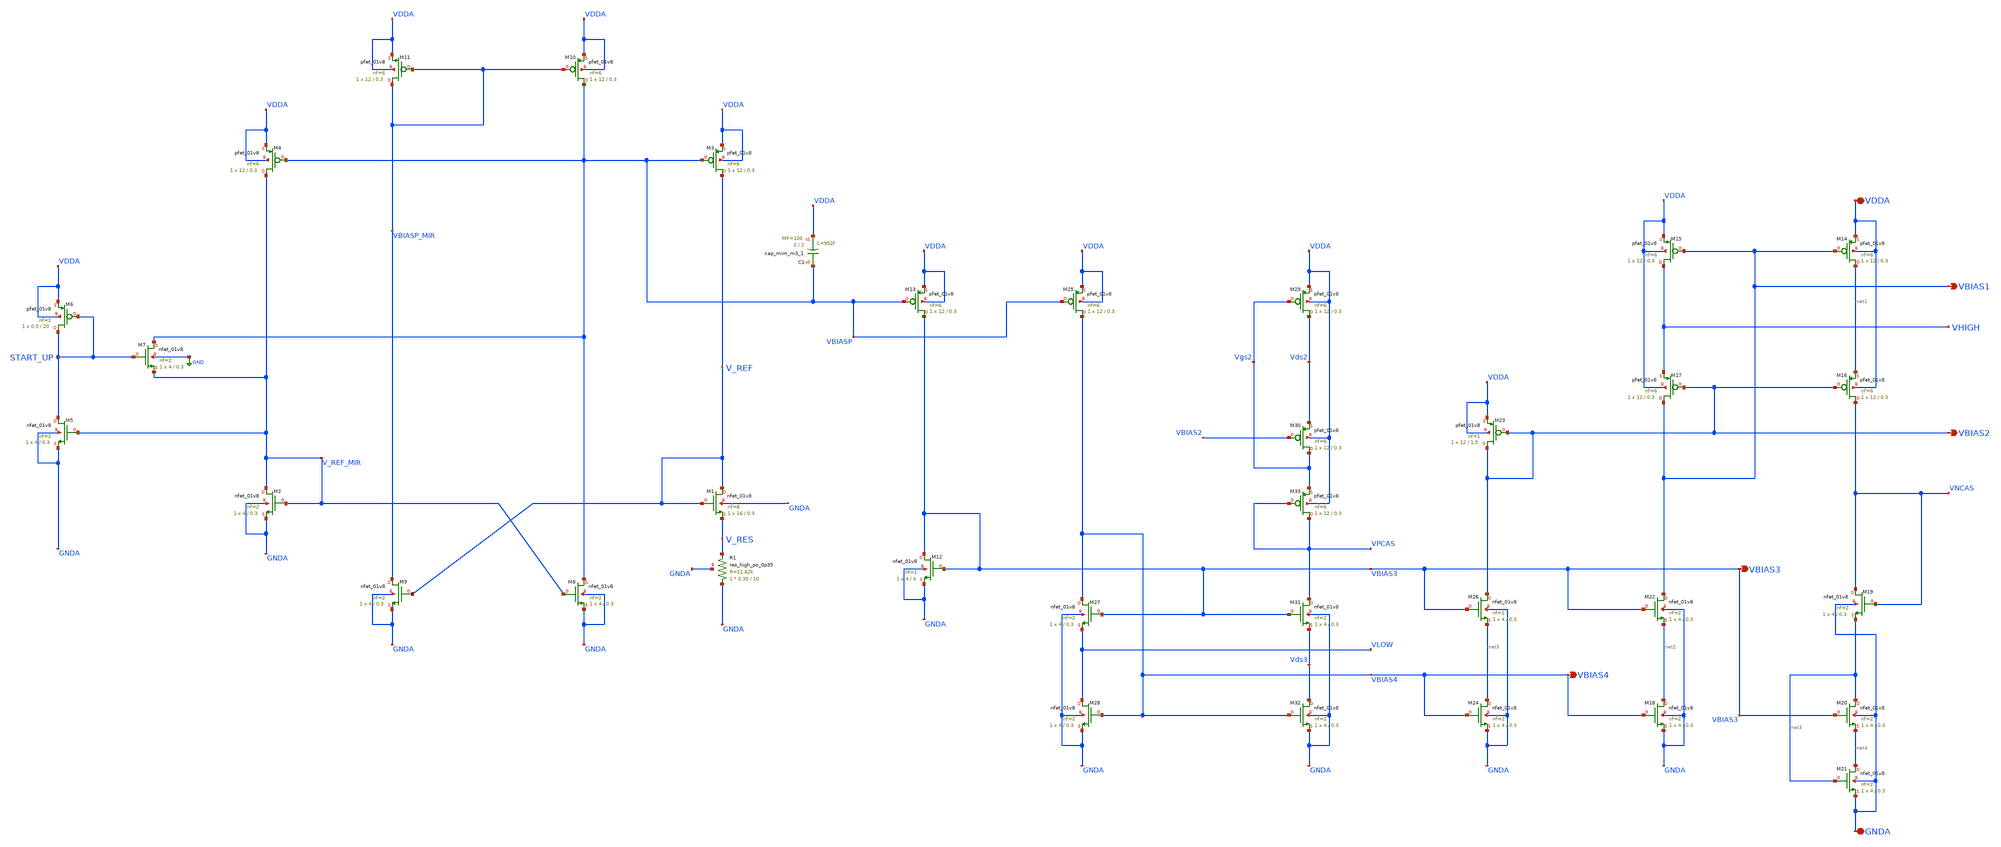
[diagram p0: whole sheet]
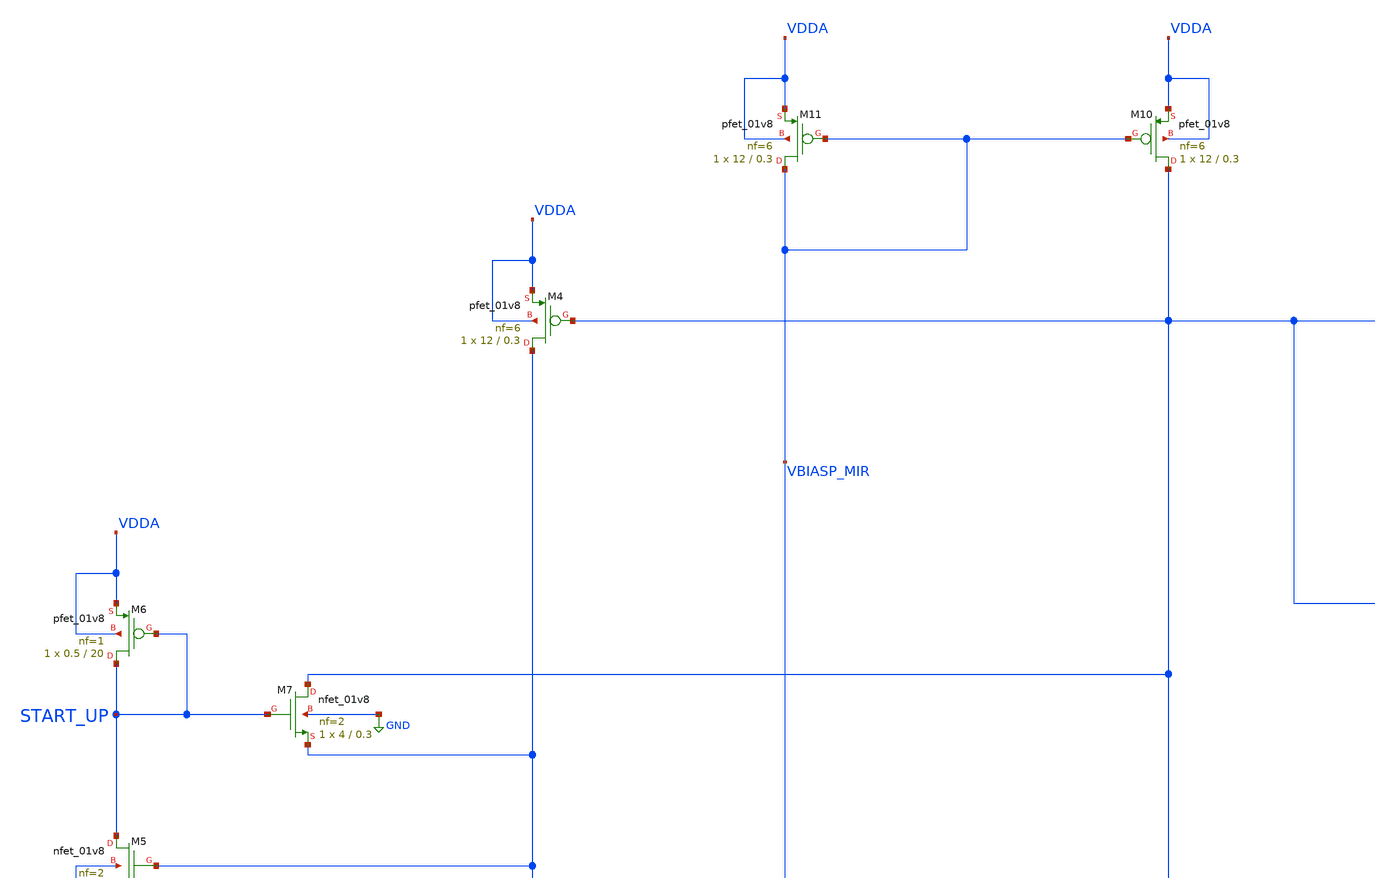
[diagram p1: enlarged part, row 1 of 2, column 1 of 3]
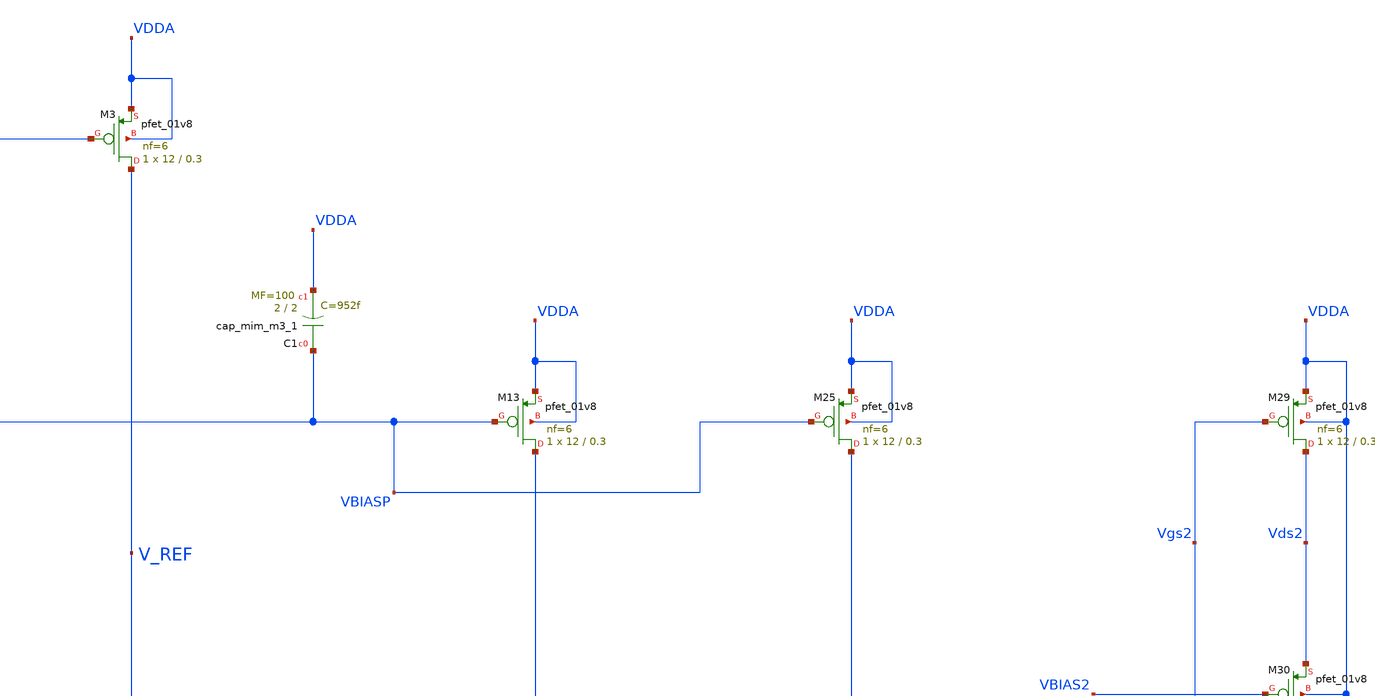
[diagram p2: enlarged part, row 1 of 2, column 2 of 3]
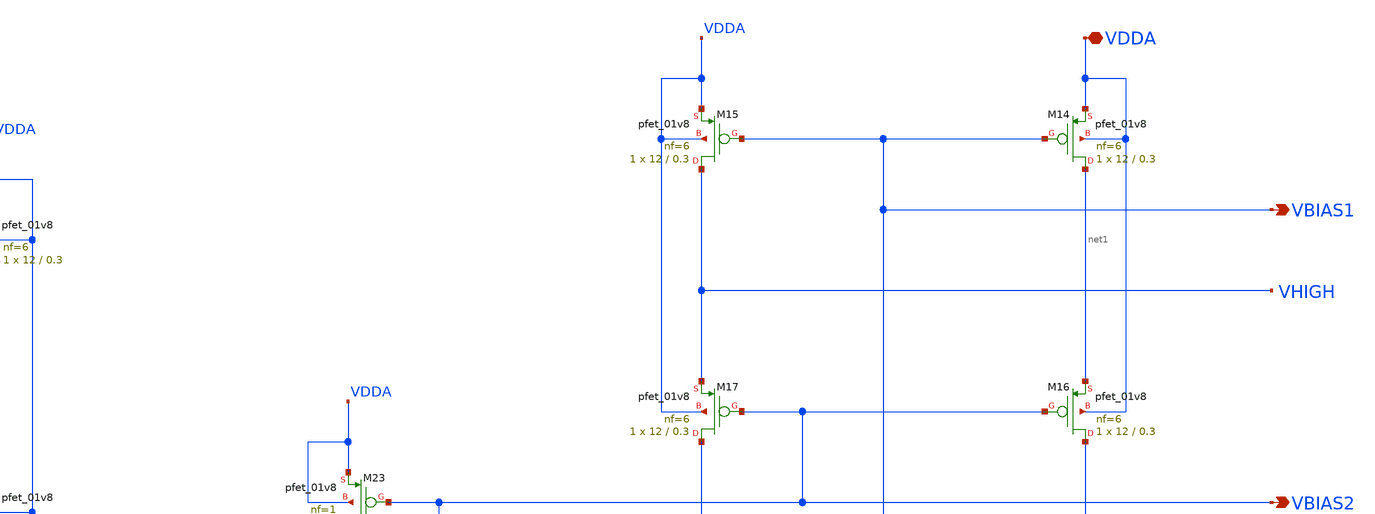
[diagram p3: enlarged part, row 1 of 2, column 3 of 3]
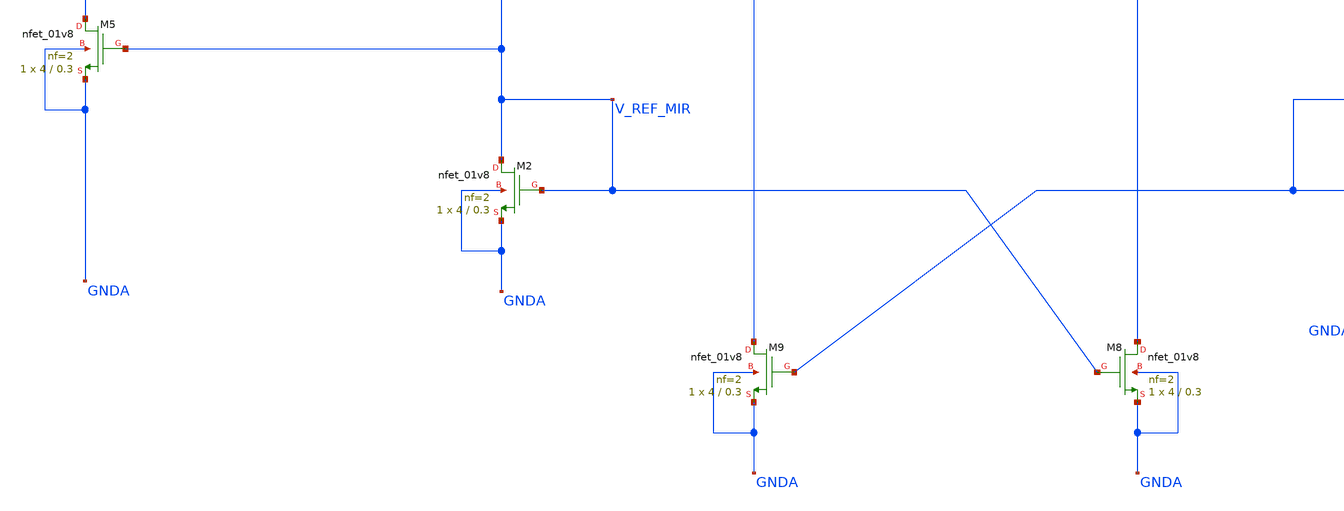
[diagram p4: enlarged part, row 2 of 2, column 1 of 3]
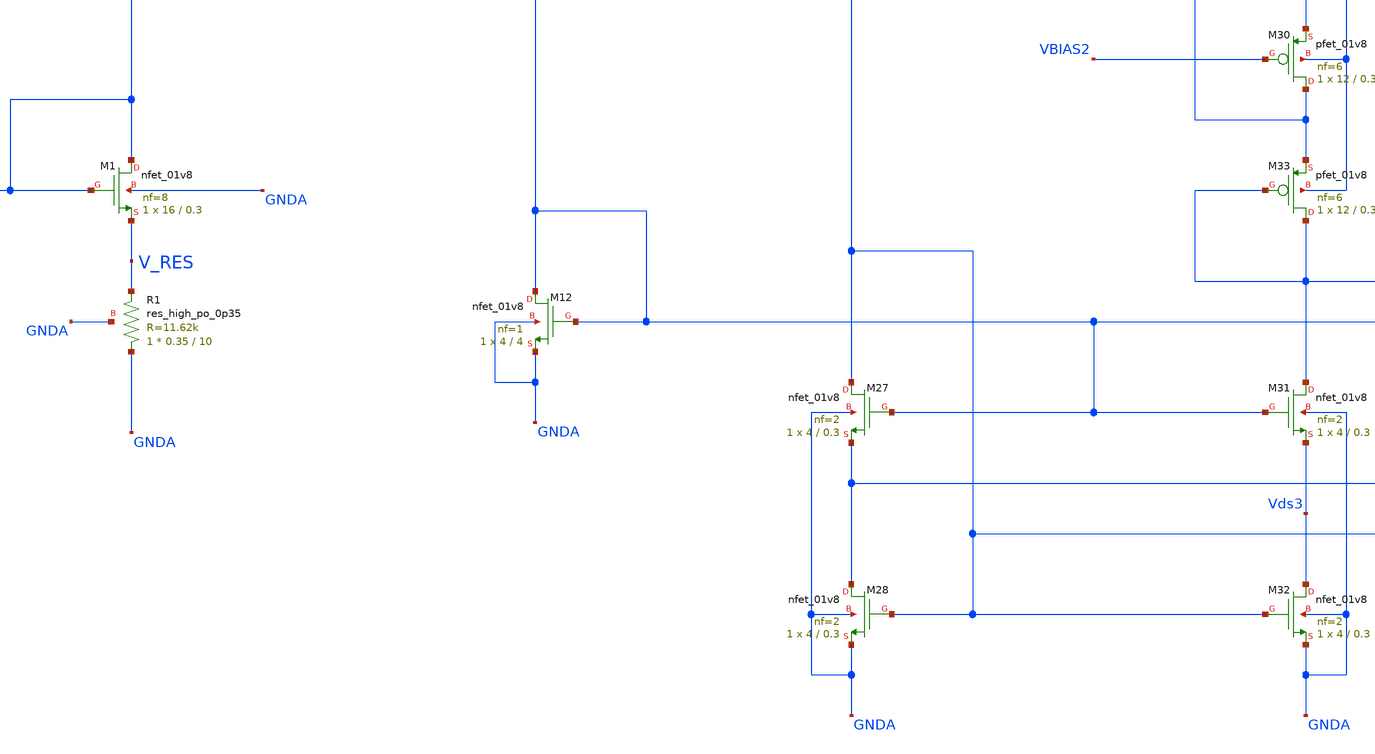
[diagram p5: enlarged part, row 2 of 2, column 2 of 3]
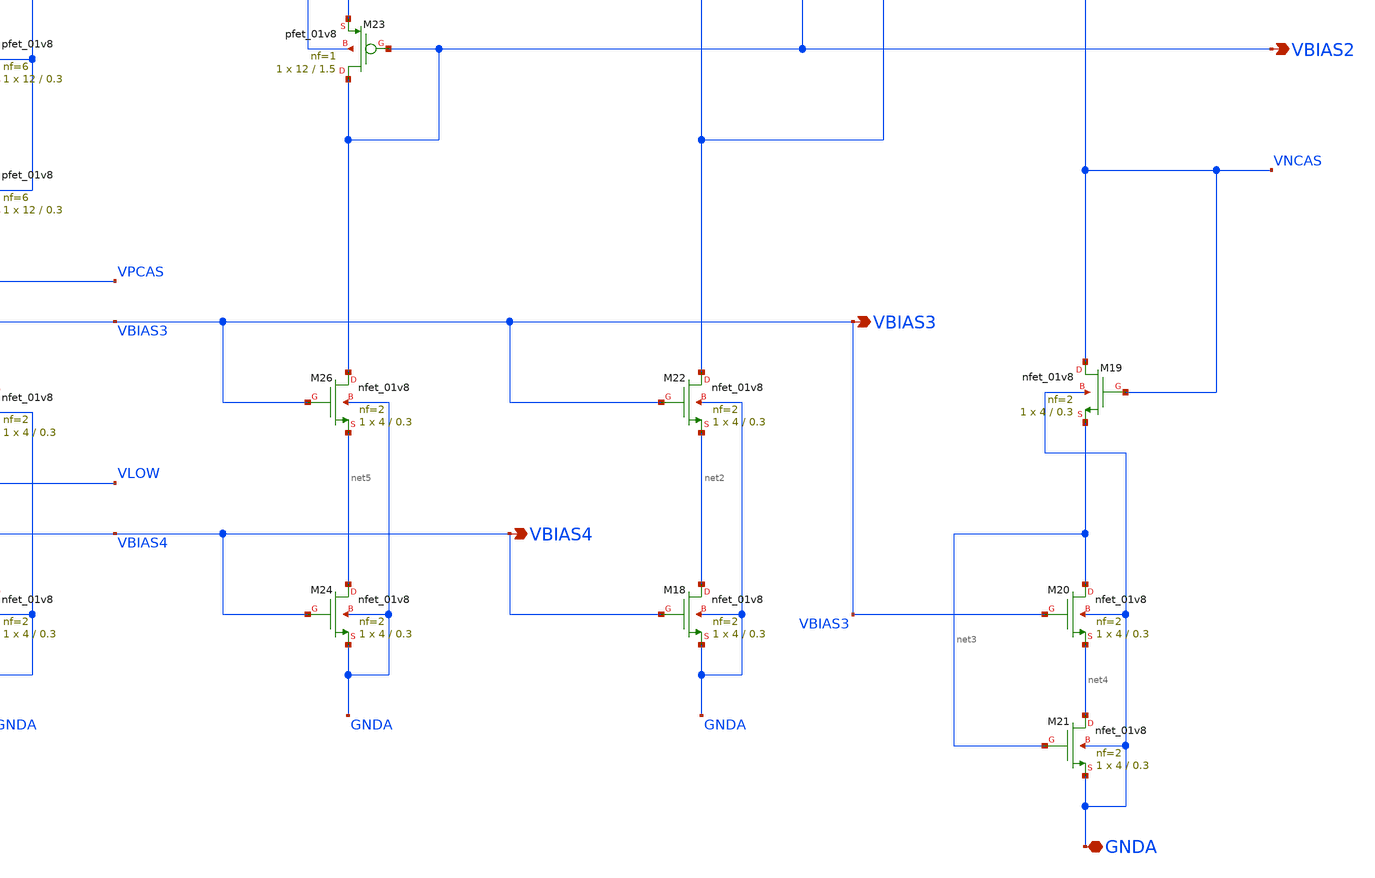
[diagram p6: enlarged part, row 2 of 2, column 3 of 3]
** sch_path: projects/ASU/EEE572/schematic/biasing_circuit.sch
**.subckt biasing_circuit VDDA GNDA VBIAS1 VBIAS2 VBIAS3 VBIAS4
*.iopin VDDA
*.iopin GNDA
*.opin VBIAS1
*.opin VBIAS2
*.opin VBIAS3
*.opin VBIAS4
XM1 V_REF V_REF V_RES GNDA sky130_fd_pr__nfet_01v8 L=0.3 W=16 nf=8 ad='int((nf+1)/2) * W/nf * 0.29' as='int((nf+2)/2) * W/nf * 0.29'
+ pd='2*int((nf+1)/2) * (W/nf + 0.29)' ps='2*int((nf+2)/2) * (W/nf + 0.29)' nrd='0.29 / W' nrs='0.29 / W'
+ sa=0 sb=0 sd=0 mult=1 m=1
XM2 V_REF_MIR V_REF_MIR GNDA GNDA sky130_fd_pr__nfet_01v8 L=0.3 W=4 nf=2 ad='int((nf+1)/2) * W/nf * 0.29'
+ as='int((nf+2)/2) * W/nf * 0.29' pd='2*int((nf+1)/2) * (W/nf + 0.29)' ps='2*int((nf+2)/2) * (W/nf + 0.29)'
+ nrd='0.29 / W' nrs='0.29 / W' sa=0 sb=0 sd=0 mult=1 m=1
XM5 START_UP V_REF_MIR GNDA GNDA sky130_fd_pr__nfet_01v8 L=0.3 W=4 nf=2 ad='int((nf+1)/2) * W/nf * 0.29'
+ as='int((nf+2)/2) * W/nf * 0.29' pd='2*int((nf+1)/2) * (W/nf + 0.29)' ps='2*int((nf+2)/2) * (W/nf + 0.29)'
+ nrd='0.29 / W' nrs='0.29 / W' sa=0 sb=0 sd=0 mult=1 m=1
XM7 VBIASP START_UP V_REF_MIR GND sky130_fd_pr__nfet_01v8 L=0.3 W=4 nf=2 ad='int((nf+1)/2) * W/nf * 0.29'
+ as='int((nf+2)/2) * W/nf * 0.29' pd='2*int((nf+1)/2) * (W/nf + 0.29)' ps='2*int((nf+2)/2) * (W/nf + 0.29)'
+ nrd='0.29 / W' nrs='0.29 / W' sa=0 sb=0 sd=0 mult=1 m=1
XM6 START_UP START_UP VDDA VDDA sky130_fd_pr__pfet_01v8 L=20 W=0.5 nf=1 ad='int((nf+1)/2) * W/nf * 0.29'
+ as='int((nf+2)/2) * W/nf * 0.29' pd='2*int((nf+1)/2) * (W/nf + 0.29)' ps='2*int((nf+2)/2) * (W/nf + 0.29)'
+ nrd='0.29 / W' nrs='0.29 / W' sa=0 sb=0 sd=0 mult=1 m=1
XM3 V_REF VBIASP VDDA VDDA sky130_fd_pr__pfet_01v8 L=0.3 W=12 nf=6 ad='int((nf+1)/2) * W/nf * 0.29' as='int((nf+2)/2) * W/nf * 0.29'
+ pd='2*int((nf+1)/2) * (W/nf + 0.29)' ps='2*int((nf+2)/2) * (W/nf + 0.29)' nrd='0.29 / W' nrs='0.29 / W'
+ sa=0 sb=0 sd=0 mult=1 m=1
XM4 V_REF_MIR VBIASP VDDA VDDA sky130_fd_pr__pfet_01v8 L=0.3 W=12 nf=6 ad='int((nf+1)/2) * W/nf * 0.29'
+ as='int((nf+2)/2) * W/nf * 0.29' pd='2*int((nf+1)/2) * (W/nf + 0.29)' ps='2*int((nf+2)/2) * (W/nf + 0.29)'
+ nrd='0.29 / W' nrs='0.29 / W' sa=0 sb=0 sd=0 mult=1 m=1
XM8 VBIASP V_REF_MIR GNDA GNDA sky130_fd_pr__nfet_01v8 L=0.3 W=4 nf=2 ad='int((nf+1)/2) * W/nf * 0.29'
+ as='int((nf+2)/2) * W/nf * 0.29' pd='2*int((nf+1)/2) * (W/nf + 0.29)' ps='2*int((nf+2)/2) * (W/nf + 0.29)'
+ nrd='0.29 / W' nrs='0.29 / W' sa=0 sb=0 sd=0 mult=1 m=1
XM9 VBIASP_MIR V_REF GNDA GNDA sky130_fd_pr__nfet_01v8 L=0.3 W=4 nf=2 ad='int((nf+1)/2) * W/nf * 0.29'
+ as='int((nf+2)/2) * W/nf * 0.29' pd='2*int((nf+1)/2) * (W/nf + 0.29)' ps='2*int((nf+2)/2) * (W/nf + 0.29)'
+ nrd='0.29 / W' nrs='0.29 / W' sa=0 sb=0 sd=0 mult=1 m=1
XM10 VBIASP VBIASP_MIR VDDA VDDA sky130_fd_pr__pfet_01v8 L=0.3 W=12 nf=6 ad='int((nf+1)/2) * W/nf * 0.29'
+ as='int((nf+2)/2) * W/nf * 0.29' pd='2*int((nf+1)/2) * (W/nf + 0.29)' ps='2*int((nf+2)/2) * (W/nf + 0.29)'
+ nrd='0.29 / W' nrs='0.29 / W' sa=0 sb=0 sd=0 mult=1 m=1
XM11 VBIASP_MIR VBIASP_MIR VDDA VDDA sky130_fd_pr__pfet_01v8 L=0.3 W=12 nf=6 ad='int((nf+1)/2) * W/nf * 0.29'
+ as='int((nf+2)/2) * W/nf * 0.29' pd='2*int((nf+1)/2) * (W/nf + 0.29)' ps='2*int((nf+2)/2) * (W/nf + 0.29)'
+ nrd='0.29 / W' nrs='0.29 / W' sa=0 sb=0 sd=0 mult=1 m=1
XM12 VBIAS3 VBIAS3 GNDA GNDA sky130_fd_pr__nfet_01v8 L=4 W=4 nf=1 ad='int((nf+1)/2) * W/nf * 0.29' as='int((nf+2)/2) * W/nf * 0.29'
+ pd='2*int((nf+1)/2) * (W/nf + 0.29)' ps='2*int((nf+2)/2) * (W/nf + 0.29)' nrd='0.29 / W' nrs='0.29 / W'
+ sa=0 sb=0 sd=0 mult=1 m=1
XM13 VBIAS3 VBIASP VDDA VDDA sky130_fd_pr__pfet_01v8 L=0.3 W=12 nf=6 ad='int((nf+1)/2) * W/nf * 0.29'
+ as='int((nf+2)/2) * W/nf * 0.29' pd='2*int((nf+1)/2) * (W/nf + 0.29)' ps='2*int((nf+2)/2) * (W/nf + 0.29)'
+ nrd='0.29 / W' nrs='0.29 / W' sa=0 sb=0 sd=0 mult=1 m=1
XM14 net1 VBIAS1 VDDA VDDA sky130_fd_pr__pfet_01v8 L=0.3 W=12 nf=6 ad='int((nf+1)/2) * W/nf * 0.29' as='int((nf+2)/2) * W/nf * 0.29'
+ pd='2*int((nf+1)/2) * (W/nf + 0.29)' ps='2*int((nf+2)/2) * (W/nf + 0.29)' nrd='0.29 / W' nrs='0.29 / W'
+ sa=0 sb=0 sd=0 mult=1 m=1
XM15 VHIGH VBIAS1 VDDA VDDA sky130_fd_pr__pfet_01v8 L=0.3 W=12 nf=6 ad='int((nf+1)/2) * W/nf * 0.29'
+ as='int((nf+2)/2) * W/nf * 0.29' pd='2*int((nf+1)/2) * (W/nf + 0.29)' ps='2*int((nf+2)/2) * (W/nf + 0.29)'
+ nrd='0.29 / W' nrs='0.29 / W' sa=0 sb=0 sd=0 mult=1 m=1
XM16 VNCAS VBIAS2 net1 VDDA sky130_fd_pr__pfet_01v8 L=0.3 W=12 nf=6 ad='int((nf+1)/2) * W/nf * 0.29'
+ as='int((nf+2)/2) * W/nf * 0.29' pd='2*int((nf+1)/2) * (W/nf + 0.29)' ps='2*int((nf+2)/2) * (W/nf + 0.29)'
+ nrd='0.29 / W' nrs='0.29 / W' sa=0 sb=0 sd=0 mult=1 m=1
XM17 VBIAS1 VBIAS2 VHIGH VDDA sky130_fd_pr__pfet_01v8 L=0.3 W=12 nf=6 ad='int((nf+1)/2) * W/nf * 0.29'
+ as='int((nf+2)/2) * W/nf * 0.29' pd='2*int((nf+1)/2) * (W/nf + 0.29)' ps='2*int((nf+2)/2) * (W/nf + 0.29)'
+ nrd='0.29 / W' nrs='0.29 / W' sa=0 sb=0 sd=0 mult=1 m=1
XM18 net2 VBIAS4 GNDA GNDA sky130_fd_pr__nfet_01v8 L=0.3 W=4 nf=2 ad='int((nf+1)/2) * W/nf * 0.29' as='int((nf+2)/2) * W/nf * 0.29'
+ pd='2*int((nf+1)/2) * (W/nf + 0.29)' ps='2*int((nf+2)/2) * (W/nf + 0.29)' nrd='0.29 / W' nrs='0.29 / W'
+ sa=0 sb=0 sd=0 mult=1 m=1
XM19 VNCAS VNCAS net3 GNDA sky130_fd_pr__nfet_01v8 L=0.3 W=4 nf=2 ad='int((nf+1)/2) * W/nf * 0.29' as='int((nf+2)/2) * W/nf * 0.29'
+ pd='2*int((nf+1)/2) * (W/nf + 0.29)' ps='2*int((nf+2)/2) * (W/nf + 0.29)' nrd='0.29 / W' nrs='0.29 / W'
+ sa=0 sb=0 sd=0 mult=1 m=1
XM20 net3 VBIAS3 net4 GNDA sky130_fd_pr__nfet_01v8 L=0.3 W=4 nf=2 ad='int((nf+1)/2) * W/nf * 0.29' as='int((nf+2)/2) * W/nf * 0.29'
+ pd='2*int((nf+1)/2) * (W/nf + 0.29)' ps='2*int((nf+2)/2) * (W/nf + 0.29)' nrd='0.29 / W' nrs='0.29 / W'
+ sa=0 sb=0 sd=0 mult=1 m=1
XM21 net4 net3 GNDA GNDA sky130_fd_pr__nfet_01v8 L=0.3 W=4 nf=2 ad='int((nf+1)/2) * W/nf * 0.29' as='int((nf+2)/2) * W/nf * 0.29'
+ pd='2*int((nf+1)/2) * (W/nf + 0.29)' ps='2*int((nf+2)/2) * (W/nf + 0.29)' nrd='0.29 / W' nrs='0.29 / W'
+ sa=0 sb=0 sd=0 mult=1 m=1
XM25 VBIAS4 VBIASP VDDA VDDA sky130_fd_pr__pfet_01v8 L=0.3 W=12 nf=6 ad='int((nf+1)/2) * W/nf * 0.29'
+ as='int((nf+2)/2) * W/nf * 0.29' pd='2*int((nf+1)/2) * (W/nf + 0.29)' ps='2*int((nf+2)/2) * (W/nf + 0.29)'
+ nrd='0.29 / W' nrs='0.29 / W' sa=0 sb=0 sd=0 mult=1 m=1
XM27 VBIAS4 VBIAS3 VLOW GNDA sky130_fd_pr__nfet_01v8 L=0.3 W=4 nf=2 ad='int((nf+1)/2) * W/nf * 0.29'
+ as='int((nf+2)/2) * W/nf * 0.29' pd='2*int((nf+1)/2) * (W/nf + 0.29)' ps='2*int((nf+2)/2) * (W/nf + 0.29)'
+ nrd='0.29 / W' nrs='0.29 / W' sa=0 sb=0 sd=0 mult=1 m=1
XM28 VLOW VBIAS4 GNDA GNDA sky130_fd_pr__nfet_01v8 L=0.3 W=4 nf=2 ad='int((nf+1)/2) * W/nf * 0.29' as='int((nf+2)/2) * W/nf * 0.29'
+ pd='2*int((nf+1)/2) * (W/nf + 0.29)' ps='2*int((nf+2)/2) * (W/nf + 0.29)' nrd='0.29 / W' nrs='0.29 / W'
+ sa=0 sb=0 sd=0 mult=1 m=1
XM29 Vds2 Vgs2 VDDA VDDA sky130_fd_pr__pfet_01v8 L=0.3 W=12 nf=6 ad='int((nf+1)/2) * W/nf * 0.29' as='int((nf+2)/2) * W/nf * 0.29'
+ pd='2*int((nf+1)/2) * (W/nf + 0.29)' ps='2*int((nf+2)/2) * (W/nf + 0.29)' nrd='0.29 / W' nrs='0.29 / W'
+ sa=0 sb=0 sd=0 mult=1 m=1
XM30 Vgs2 VBIAS2 Vds2 VDDA sky130_fd_pr__pfet_01v8 L=0.3 W=12 nf=6 ad='int((nf+1)/2) * W/nf * 0.29' as='int((nf+2)/2) * W/nf * 0.29'
+ pd='2*int((nf+1)/2) * (W/nf + 0.29)' ps='2*int((nf+2)/2) * (W/nf + 0.29)' nrd='0.29 / W' nrs='0.29 / W'
+ sa=0 sb=0 sd=0 mult=1 m=1
XM31 VPCAS VBIAS3 Vds3 GNDA sky130_fd_pr__nfet_01v8 L=0.3 W=4 nf=2 ad='int((nf+1)/2) * W/nf * 0.29' as='int((nf+2)/2) * W/nf * 0.29'
+ pd='2*int((nf+1)/2) * (W/nf + 0.29)' ps='2*int((nf+2)/2) * (W/nf + 0.29)' nrd='0.29 / W' nrs='0.29 / W'
+ sa=0 sb=0 sd=0 mult=1 m=1
XM32 Vds3 VBIAS4 GNDA GNDA sky130_fd_pr__nfet_01v8 L=0.3 W=4 nf=2 ad='int((nf+1)/2) * W/nf * 0.29' as='int((nf+2)/2) * W/nf * 0.29'
+ pd='2*int((nf+1)/2) * (W/nf + 0.29)' ps='2*int((nf+2)/2) * (W/nf + 0.29)' nrd='0.29 / W' nrs='0.29 / W'
+ sa=0 sb=0 sd=0 mult=1 m=1
XM33 VPCAS VPCAS Vgs2 VDDA sky130_fd_pr__pfet_01v8 L=0.3 W=12 nf=6 ad='int((nf+1)/2) * W/nf * 0.29' as='int((nf+2)/2) * W/nf * 0.29'
+ pd='2*int((nf+1)/2) * (W/nf + 0.29)' ps='2*int((nf+2)/2) * (W/nf + 0.29)' nrd='0.29 / W' nrs='0.29 / W'
+ sa=0 sb=0 sd=0 mult=1 m=1
XM22 VBIAS1 VBIAS3 net2 GNDA sky130_fd_pr__nfet_01v8 L=0.3 W=4 nf=2 ad='int((nf+1)/2) * W/nf * 0.29'
+ as='int((nf+2)/2) * W/nf * 0.29' pd='2*int((nf+1)/2) * (W/nf + 0.29)' ps='2*int((nf+2)/2) * (W/nf + 0.29)'
+ nrd='0.29 / W' nrs='0.29 / W' sa=0 sb=0 sd=0 mult=1 m=1
XM23 VBIAS2 VBIAS2 VDDA VDDA sky130_fd_pr__pfet_01v8 L=1.5 W=12 nf=1 ad='int((nf+1)/2) * W/nf * 0.29'
+ as='int((nf+2)/2) * W/nf * 0.29' pd='2*int((nf+1)/2) * (W/nf + 0.29)' ps='2*int((nf+2)/2) * (W/nf + 0.29)'
+ nrd='0.29 / W' nrs='0.29 / W' sa=0 sb=0 sd=0 mult=1 m=1
XM24 net5 VBIAS4 GNDA GNDA sky130_fd_pr__nfet_01v8 L=0.3 W=4 nf=2 ad='int((nf+1)/2) * W/nf * 0.29' as='int((nf+2)/2) * W/nf * 0.29'
+ pd='2*int((nf+1)/2) * (W/nf + 0.29)' ps='2*int((nf+2)/2) * (W/nf + 0.29)' nrd='0.29 / W' nrs='0.29 / W'
+ sa=0 sb=0 sd=0 mult=1 m=1
XM26 VBIAS2 VBIAS3 net5 GNDA sky130_fd_pr__nfet_01v8 L=0.3 W=4 nf=2 ad='int((nf+1)/2) * W/nf * 0.29'
+ as='int((nf+2)/2) * W/nf * 0.29' pd='2*int((nf+1)/2) * (W/nf + 0.29)' ps='2*int((nf+2)/2) * (W/nf + 0.29)'
+ nrd='0.29 / W' nrs='0.29 / W' sa=0 sb=0 sd=0 mult=1 m=1
XR1 GNDA V_RES GNDA sky130_fd_pr__res_high_po_0p35 L=10 mult=1 m=1
XC1 VBIASP VDDA sky130_fd_pr__cap_mim_m3_1 W=2 L=2 MF=100 m=100
**.ends
.GLOBAL GND
.end
